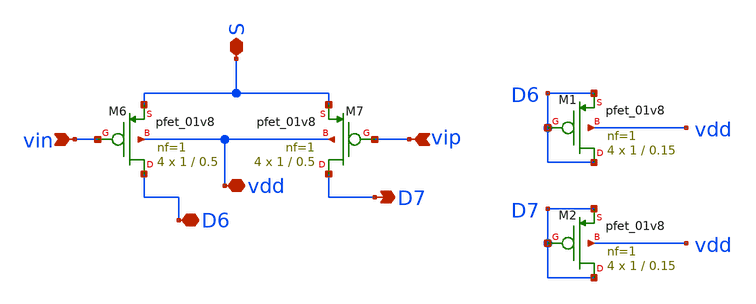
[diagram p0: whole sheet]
** sch_path: pmos_diff.sch
**.subckt pmos_diff vin vip D7 D6 vdd S
*.ipin vin
*.ipin vip
*.opin D7
*.iopin D6
*.iopin vdd
*.iopin S
XM6 D6 vin S vdd sky130_fd_pr__pfet_01v8 L=0.5 W=1 nf=1 ad='int((nf+1)/2) * W/nf * 0.29' as='int((nf+2)/2) * W/nf * 0.29'
+ pd='2*int((nf+1)/2) * (W/nf + 0.29)' ps='2*int((nf+2)/2) * (W/nf + 0.29)' nrd='0.29 / W' nrs='0.29 / W'
+ sa=0 sb=0 sd=0 mult=4 m=4
XM7 D7 vip S vdd sky130_fd_pr__pfet_01v8 L=0.5 W=1 nf=1 ad='int((nf+1)/2) * W/nf * 0.29' as='int((nf+2)/2) * W/nf * 0.29'
+ pd='2*int((nf+1)/2) * (W/nf + 0.29)' ps='2*int((nf+2)/2) * (W/nf + 0.29)' nrd='0.29 / W' nrs='0.29 / W'
+ sa=0 sb=0 sd=0 mult=4 m=4
XM1 D6 D6 D6 vdd sky130_fd_pr__pfet_01v8 L=0.15 W=1 nf=1 ad='int((nf+1)/2) * W/nf * 0.29' as='int((nf+2)/2) * W/nf * 0.29'
+ pd='2*int((nf+1)/2) * (W/nf + 0.29)' ps='2*int((nf+2)/2) * (W/nf + 0.29)' nrd='0.29 / W' nrs='0.29 / W'
+ sa=0 sb=0 sd=0 mult=4 m=4
XM2 D7 D7 D7 vdd sky130_fd_pr__pfet_01v8 L=0.15 W=1 nf=1 ad='int((nf+1)/2) * W/nf * 0.29' as='int((nf+2)/2) * W/nf * 0.29'
+ pd='2*int((nf+1)/2) * (W/nf + 0.29)' ps='2*int((nf+2)/2) * (W/nf + 0.29)' nrd='0.29 / W' nrs='0.29 / W'
+ sa=0 sb=0 sd=0 mult=4 m=4
**.ends
.end
